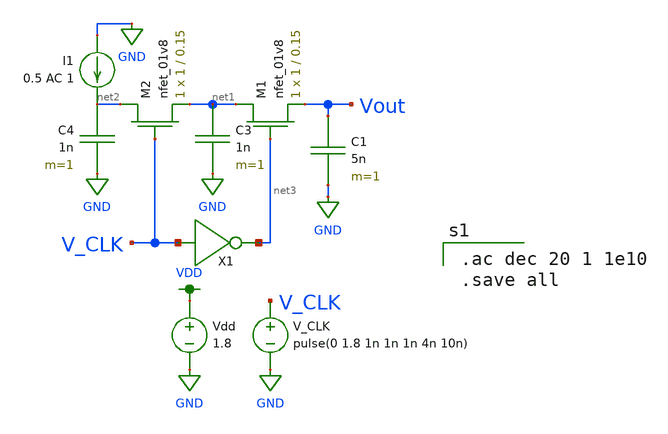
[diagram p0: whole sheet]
** sch_path: simulation/filter/filter_tran.sch
**.subckt filter_tran
Vdd VDD GND 1.8
V_CLK V_CLK GND pulse(0 1.8 1n 1n 1n 4n 10n)
C1 Vout GND 5n m=1
I1 GND net2 0.5 AC 1
C3 net1 GND 1n m=1
XM1 net1 net3 Vout GND sky130_fd_pr__nfet_01v8 L=0.15 W=1 nf=1 ad='int((nf+1)/2) * W/nf * 0.29' as='int((nf+2)/2) * W/nf * 0.29'
+ pd='2*int((nf+1)/2) * (W/nf + 0.29)' ps='2*int((nf+2)/2) * (W/nf + 0.29)' nrd='0.29 / W' nrs='0.29 / W'
+ sa=0 sb=0 sd=0 mult=1 m=1
XM2 net2 V_CLK net1 GND sky130_fd_pr__nfet_01v8 L=0.15 W=1 nf=1 ad='int((nf+1)/2) * W/nf * 0.29' as='int((nf+2)/2) * W/nf * 0.29'
+ pd='2*int((nf+1)/2) * (W/nf + 0.29)' ps='2*int((nf+2)/2) * (W/nf + 0.29)' nrd='0.29 / W' nrs='0.29 / W'
+ sa=0 sb=0 sd=0 mult=1 m=1
C4 net2 GND 1n m=1
X1 V_CLK net3 inverter
**** begin user architecture code

.ac dec 20 1 1e10
.save all


.option wnflag=1
.param MC_SWITCH=0.0
.lib ~/skywater/skywater-pdk/libraries/sky130_fd_pr_ngspice/latest/models/sky130.lib.spice tt

**** end user architecture code
**.ends

* expanding   symbol:  /home/madvlsi/VLSI_Sine_Gen/simulation/dac/inverter.sym # of pins=2
** sym_path: simulation/dac/inverter.sym
** sch_path: simulation/dac/inverter.sch
.subckt inverter A Y
*.ipin A
*.opin Y
XM1 Y A VDD VDD sky130_fd_pr__pfet_01v8 L=0.15 W=1 nf=1 ad='int((nf+1)/2) * W/nf * 0.29' as='int((nf+2)/2) * W/nf * 0.29'
+ pd='2*int((nf+1)/2) * (W/nf + 0.29)' ps='2*int((nf+2)/2) * (W/nf + 0.29)' nrd='0.29 / W' nrs='0.29 / W'
+ sa=0 sb=0 sd=0 mult=1 m=1
XM2 Y A GND GND sky130_fd_pr__nfet_01v8 L=0.15 W=1 nf=1 ad='int((nf+1)/2) * W/nf * 0.29' as='int((nf+2)/2) * W/nf * 0.29'
+ pd='2*int((nf+1)/2) * (W/nf + 0.29)' ps='2*int((nf+2)/2) * (W/nf + 0.29)' nrd='0.29 / W' nrs='0.29 / W'
+ sa=0 sb=0 sd=0 mult=1 m=1
.ends

.GLOBAL GND
.GLOBAL VDD
.end
